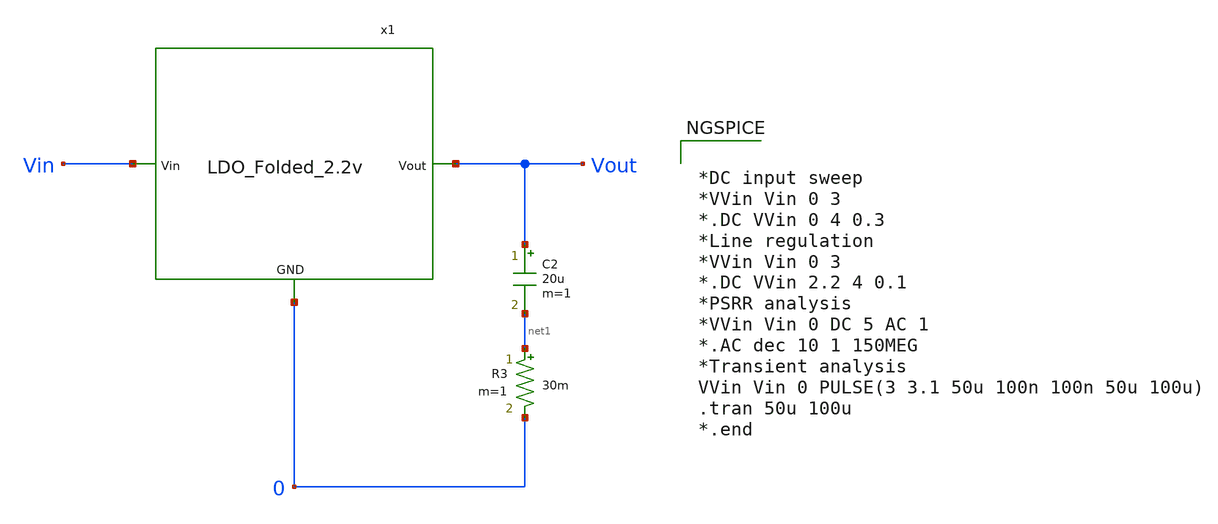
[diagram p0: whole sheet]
** sch_path: Analog_Blocks/LDO/Testbench/LDO_Folded_2.2v_TB.sch
**.subckt LDO_Folded_2.2v_TB
C2 Vout net1 20u m=1
R3 net1 0 30m m=1
x1 Vin Vout 0 LDO_Folded_2.2v
**** begin user architecture code


*DC input sweep
*VVin Vin 0 3
*.DC VVin 0 4 0.3
*Line regulation
*VVin Vin 0 3
*.DC VVin 2.2 4 0.1
*PSRR analysis
*VVin Vin 0 DC 5 AC 1
*.AC dec 10 1 150MEG
*Transient analysis
VVin Vin 0 PULSE(3 3.1 50u 100n 100n 50u 100u)
.tran 50u 100u
*.end



.include $::SKYWATER_MODELS/cells/nfet_01v8/sky130_fd_pr__nfet_01v8__tt.corner.spice
.include $::SKYWATER_MODELS/cells/nfet_01v8_lvt/sky130_fd_pr__nfet_01v8_lvt__tt.corner.spice
.include $::SKYWATER_MODELS/cells/pfet_01v8/sky130_fd_pr__pfet_01v8__tt.corner.spice
.include $::SKYWATER_MODELS/cells/nfet_03v3_nvt/sky130_fd_pr__nfet_03v3_nvt__tt.corner.spice
.include $::SKYWATER_MODELS/cells/nfet_05v0_nvt/sky130_fd_pr__nfet_05v0_nvt__tt.corner.spice
.include $::SKYWATER_MODELS/cells/esd_nfet_01v8/sky130_fd_pr__esd_nfet_01v8__tt.corner.spice
.include $::SKYWATER_MODELS/cells/pfet_01v8_lvt/sky130_fd_pr__pfet_01v8_lvt__tt.corner.spice
.include $::SKYWATER_MODELS/cells/pfet_01v8_hvt/sky130_fd_pr__pfet_01v8_hvt__tt.corner.spice
.include $::SKYWATER_MODELS/cells/esd_pfet_g5v0d10v5/sky130_fd_pr__esd_pfet_g5v0d10v5__tt.corner.spice
.include $::SKYWATER_MODELS/cells/pfet_g5v0d10v5/sky130_fd_pr__pfet_g5v0d10v5__tt.corner.spice
.include $::SKYWATER_MODELS/cells/pfet_g5v0d16v0/sky130_fd_pr__pfet_g5v0d16v0__tt.corner.spice
.include $::SKYWATER_MODELS/cells/nfet_g5v0d10v5/sky130_fd_pr__nfet_g5v0d10v5__tt.corner.spice
.include $::SKYWATER_MODELS/cells/nfet_g5v0d16v0/sky130_fd_pr__nfet_g5v0d16v0__tt_discrete.corner.spice
.include $::SKYWATER_MODELS/cells/esd_nfet_g5v0d10v5/sky130_fd_pr__esd_nfet_g5v0d10v5__tt.corner.spice
.include $::SKYWATER_MODELS/models/corners/tt/nonfet.spice
* Mismatch parameters
.include $::SKYWATER_MODELS/cells/nfet_01v8/sky130_fd_pr__nfet_01v8__mismatch.corner.spice
.include $::SKYWATER_MODELS/cells/pfet_01v8/sky130_fd_pr__pfet_01v8__mismatch.corner.spice
.include $::SKYWATER_MODELS/cells/nfet_01v8_lvt/sky130_fd_pr__nfet_01v8_lvt__mismatch.corner.spice
.include $::SKYWATER_MODELS/cells/pfet_01v8_lvt/sky130_fd_pr__pfet_01v8_lvt__mismatch.corner.spice
.include $::SKYWATER_MODELS/cells/pfet_01v8_hvt/sky130_fd_pr__pfet_01v8_hvt__mismatch.corner.spice
.include $::SKYWATER_MODELS/cells/nfet_g5v0d10v5/sky130_fd_pr__nfet_g5v0d10v5__mismatch.corner.spice
.include $::SKYWATER_MODELS/cells/pfet_g5v0d10v5/sky130_fd_pr__pfet_g5v0d10v5__mismatch.corner.spice
.include $::SKYWATER_MODELS/cells/nfet_05v0_nvt/sky130_fd_pr__nfet_05v0_nvt__mismatch.corner.spice
.include $::SKYWATER_MODELS/cells/nfet_03v3_nvt/sky130_fd_pr__nfet_03v3_nvt__mismatch.corner.spice
* Resistor$::SKYWATER_MODELS/Capacitor
.include $::SKYWATER_MODELS/models/r+c/res_typical__cap_typical.spice
.include $::SKYWATER_MODELS/models/r+c/res_typical__cap_typical__lin.spice
* Special cells
.include $::SKYWATER_MODELS/models/corners/tt/specialized_cells.spice
* All models
.include $::SKYWATER_MODELS/models/all.spice
* Corner
.include $::SKYWATER_MODELS/models/corners/tt/rf.spice

**** end user architecture code
**.ends

* expanding   symbol:
*+  /home/eslam/Analog_blocks/Analog_Blocks/LDO/Schematic/LDO_Folded_2.2v/LDO_Folded_2.2v.sym # of pins=3
** sym_path: Analog_blocks/Analog_Blocks/LDO/Schematic/LDO_Folded_2.2v/LDO_Folded_2.2v.sym
** sch_path: Analog_blocks/Analog_Blocks/LDO/Schematic/LDO_Folded_2.2v/LDO_Folded_2.2v.sch
.subckt LDO_Folded_2.2v Vin Vout GND
*.ipin Vin
*.ipin GND
*.opin Vout
XR1 net1 Vout GND sky130_fd_pr__res_xhigh_po W=1 L=60 mult=1 m=1
XR2 GND net1 GND sky130_fd_pr__res_xhigh_po W=1 L=50 mult=1 m=1
XC1 Vout net1 sky130_fd_pr__cap_mim_m3_2 W=1 L=1 MF=1 m=1
XM1 Vout net2 Vin Vin sky130_fd_pr__pfet_g5v0d10v5 L=0.5 W=20 nf=1 ad='int((nf+1)/2) * W/nf * 0.29' as='int((nf+2)/2) * W/nf * 0.29'
+ pd='2*int((nf+1)/2) * (W/nf + 0.29)' ps='2*int((nf+2)/2) * (W/nf + 0.29)' nrd='0.29 / W' nrs='0.29 / W'
+ sa=0 sb=0 sd=0 mult=1000 m=1000
x1 Vin net2 net1 net3 net3 GND Error_amplifier_Folded
x2 net3 Vin GND Bandgap5v
.ends


* expanding   symbol:
*+  /home/eslam/Analog_blocks/Analog_Blocks/LDO/Schematic/LDO_Folded_2.2v/Error_amplifier_Folded.sym # of pins=6
** sym_path: Analog_Blocks/LDO/Schematic/LDO_Folded_1.8v/Error_amplifier_Folded.sym
** sch_path: Analog_Blocks/LDO/Schematic/LDO_Folded_1.8v/Error_amplifier_Folded.sch
.subckt Error_amplifier_Folded VDD Vout Vp Vn Ibias GND
*.ipin VDD
*.ipin GND
*.ipin Vp
*.ipin Vn
*.opin Vout
*.ipin Ibias
XM1 net3 Vp net1 GND sky130_fd_pr__nfet_g5v0d10v5 L=0.5 W=50 nf=1 ad='int((nf+1)/2) * W/nf * 0.29' as='int((nf+2)/2) * W/nf * 0.29'
+ pd='2*int((nf+1)/2) * (W/nf + 0.29)' ps='2*int((nf+2)/2) * (W/nf + 0.29)' nrd='0.29 / W' nrs='0.29 / W'
+ sa=0 sb=0 sd=0 mult=1 m=1
XM2 net2 Vn net1 GND sky130_fd_pr__nfet_g5v0d10v5 L=0.5 W=50 nf=1 ad='int((nf+1)/2) * W/nf * 0.29' as='int((nf+2)/2) * W/nf * 0.29'
+ pd='2*int((nf+1)/2) * (W/nf + 0.29)' ps='2*int((nf+2)/2) * (W/nf + 0.29)' nrd='0.29 / W' nrs='0.29 / W'
+ sa=0 sb=0 sd=0 mult=1 m=1
XM9 Vout net4 GND GND sky130_fd_pr__nfet_g5v0d10v5 L=2 W=6 nf=1 ad='int((nf+1)/2) * W/nf * 0.29' as='int((nf+2)/2) * W/nf * 0.29'
+ pd='2*int((nf+1)/2) * (W/nf + 0.29)' ps='2*int((nf+2)/2) * (W/nf + 0.29)' nrd='0.29 / W' nrs='0.29 / W'
+ sa=0 sb=0 sd=0 mult=1 m=1
XM6 net4 net6 net3 VDD sky130_fd_pr__pfet_g5v0d10v5 L=0.5 W=40 nf=1 ad='int((nf+1)/2) * W/nf * 0.29'
+ as='int((nf+2)/2) * W/nf * 0.29' pd='2*int((nf+1)/2) * (W/nf + 0.29)' ps='2*int((nf+2)/2) * (W/nf + 0.29)'
+ nrd='0.29 / W' nrs='0.29 / W' sa=0 sb=0 sd=0 mult=1 m=1
XM5 net2 net5 VDD VDD sky130_fd_pr__pfet_g5v0d10v5 L=0.5 W=40 nf=1 ad='int((nf+1)/2) * W/nf * 0.29' as='int((nf+2)/2) * W/nf * 0.29'
+ pd='2*int((nf+1)/2) * (W/nf + 0.29)' ps='2*int((nf+2)/2) * (W/nf + 0.29)' nrd='0.29 / W' nrs='0.29 / W'
+ sa=0 sb=0 sd=0 mult=1 m=1
XM4 net3 net5 VDD VDD sky130_fd_pr__pfet_g5v0d10v5 L=0.5 W=40 nf=1 ad='int((nf+1)/2) * W/nf * 0.29' as='int((nf+2)/2) * W/nf * 0.29'
+ pd='2*int((nf+1)/2) * (W/nf + 0.29)' ps='2*int((nf+2)/2) * (W/nf + 0.29)' nrd='0.29 / W' nrs='0.29 / W'
+ sa=0 sb=0 sd=0 mult=1 m=1
XM3 net1 Ibias GND GND sky130_fd_pr__nfet_g5v0d10v5 L=0.9 W=12 nf=1 ad='int((nf+1)/2) * W/nf * 0.29'
+ as='int((nf+2)/2) * W/nf * 0.29' pd='2*int((nf+1)/2) * (W/nf + 0.29)' ps='2*int((nf+2)/2) * (W/nf + 0.29)'
+ nrd='0.29 / W' nrs='0.29 / W' sa=0 sb=0 sd=0 mult=1 m=1
XM7 Vout net6 net2 VDD sky130_fd_pr__pfet_g5v0d10v5 L=0.5 W=40 nf=1 ad='int((nf+1)/2) * W/nf * 0.29'
+ as='int((nf+2)/2) * W/nf * 0.29' pd='2*int((nf+1)/2) * (W/nf + 0.29)' ps='2*int((nf+2)/2) * (W/nf + 0.29)'
+ nrd='0.29 / W' nrs='0.29 / W' sa=0 sb=0 sd=0 mult=1 m=1
XM8 net4 net4 GND GND sky130_fd_pr__nfet_g5v0d10v5 L=2 W=6 nf=1 ad='int((nf+1)/2) * W/nf * 0.29' as='int((nf+2)/2) * W/nf * 0.29'
+ pd='2*int((nf+1)/2) * (W/nf + 0.29)' ps='2*int((nf+2)/2) * (W/nf + 0.29)' nrd='0.29 / W' nrs='0.29 / W'
+ sa=0 sb=0 sd=0 mult=1 m=1
XM10 Ibias Ibias GND GND sky130_fd_pr__nfet_g5v0d10v5 L=0.9 W=12 nf=1 ad='int((nf+1)/2) * W/nf * 0.29'
+ as='int((nf+2)/2) * W/nf * 0.29' pd='2*int((nf+1)/2) * (W/nf + 0.29)' ps='2*int((nf+2)/2) * (W/nf + 0.29)'
+ nrd='0.29 / W' nrs='0.29 / W' sa=0 sb=0 sd=0 mult=1 m=1
XM11 net5 Ibias GND GND sky130_fd_pr__nfet_g5v0d10v5 L=0.9 W=6 nf=1 ad='int((nf+1)/2) * W/nf * 0.29'
+ as='int((nf+2)/2) * W/nf * 0.29' pd='2*int((nf+1)/2) * (W/nf + 0.29)' ps='2*int((nf+2)/2) * (W/nf + 0.29)'
+ nrd='0.29 / W' nrs='0.29 / W' sa=0 sb=0 sd=0 mult=1 m=1
XM12 net6 Ibias GND GND sky130_fd_pr__nfet_g5v0d10v5 L=0.9 W=6 nf=1 ad='int((nf+1)/2) * W/nf * 0.29'
+ as='int((nf+2)/2) * W/nf * 0.29' pd='2*int((nf+1)/2) * (W/nf + 0.29)' ps='2*int((nf+2)/2) * (W/nf + 0.29)'
+ nrd='0.29 / W' nrs='0.29 / W' sa=0 sb=0 sd=0 mult=1 m=1
XM13 net5 net5 VDD VDD sky130_fd_pr__pfet_g5v0d10v5 L=0.5 W=13.5 nf=1 ad='int((nf+1)/2) * W/nf * 0.29'
+ as='int((nf+2)/2) * W/nf * 0.29' pd='2*int((nf+1)/2) * (W/nf + 0.29)' ps='2*int((nf+2)/2) * (W/nf + 0.29)'
+ nrd='0.29 / W' nrs='0.29 / W' sa=0 sb=0 sd=0 mult=1 m=1
XM14 net6 net6 VDD VDD sky130_fd_pr__pfet_g5v0d10v5 L=1 W=2 nf=1 ad='int((nf+1)/2) * W/nf * 0.29' as='int((nf+2)/2) * W/nf * 0.29'
+ pd='2*int((nf+1)/2) * (W/nf + 0.29)' ps='2*int((nf+2)/2) * (W/nf + 0.29)' nrd='0.29 / W' nrs='0.29 / W'
+ sa=0 sb=0 sd=0 mult=1 m=1
.ends


* expanding   symbol:
*+  /home/eslam/Analog_blocks/Analog_Blocks/LDO/Schematic/LDO_Folded_2.2v/Bandgap5v.sym # of pins=3
** sym_path: Analog_Blocks/Bandgap/Schematics/BGR5v/Bandgap5v.sym
** sch_path: Analog_Blocks/Bandgap/Schematics/BGR5v/Bandgap5v.sch
.subckt Bandgap5v Vref VDD GND
*.ipin VDD
*.ipin GND
*.opin Vref
XQ1 GND GND net3 sky130_fd_pr__pnp_05v5_W0p68L0p68 m=1
XQ2 GND GND net1 sky130_fd_pr__pnp_05v5_W0p68L0p68 m=1
XQ3 GND GND net1 sky130_fd_pr__pnp_05v5_W0p68L0p68 m=1
XQ4 GND GND net1 sky130_fd_pr__pnp_05v5_W0p68L0p68 m=1
XQ5 GND GND net1 sky130_fd_pr__pnp_05v5_W0p68L0p68 m=1
XQ6 GND GND net1 sky130_fd_pr__pnp_05v5_W0p68L0p68 m=1
XQ7 GND GND net1 sky130_fd_pr__pnp_05v5_W0p68L0p68 m=1
XQ8 GND GND net1 sky130_fd_pr__pnp_05v5_W0p68L0p68 m=1
XQ9 GND GND net1 sky130_fd_pr__pnp_05v5_W0p68L0p68 m=1
XM2 net4 net5 VDD VDD sky130_fd_pr__pfet_g5v0d10v5 L=1 W=10 nf=1 ad='int((nf+1)/2) * W/nf * 0.29' as='int((nf+2)/2) * W/nf * 0.29'
+ pd='2*int((nf+1)/2) * (W/nf + 0.29)' ps='2*int((nf+2)/2) * (W/nf + 0.29)' nrd='0.29 / W' nrs='0.29 / W'
+ sa=0 sb=0 sd=0 mult=1 m=1
XM3 net3 net4 VDD VDD sky130_fd_pr__pfet_g5v0d10v5 L=1 W=10 nf=1 ad='int((nf+1)/2) * W/nf * 0.29' as='int((nf+2)/2) * W/nf * 0.29'
+ pd='2*int((nf+1)/2) * (W/nf + 0.29)' ps='2*int((nf+2)/2) * (W/nf + 0.29)' nrd='0.29 / W' nrs='0.29 / W'
+ sa=0 sb=0 sd=0 mult=1 m=1
XM1 net4 net5 GND GND sky130_fd_pr__nfet_g5v0d10v5 L=40 W=1 nf=1 ad='int((nf+1)/2) * W/nf * 0.29' as='int((nf+2)/2) * W/nf * 0.29'
+ pd='2*int((nf+1)/2) * (W/nf + 0.29)' ps='2*int((nf+2)/2) * (W/nf + 0.29)' nrd='0.29 / W' nrs='0.29 / W'
+ sa=0 sb=0 sd=0 mult=1 m=1
XR1 net2 Vref GND sky130_fd_pr__res_high_po W=1 L=6 mult=1 m=1
XR3 net3 Vref GND sky130_fd_pr__res_high_po W=1 L=6 mult=1 m=1
XR2 net1 net2 GND sky130_fd_pr__res_high_po W=1 L=2.6 mult=1 m=1
x1 VDD net3 net2 Vref net5 GND Bandgap5v_OTA
.ends


* expanding   symbol:
*+  /home/eslam/Analog_blocks/Analog_Blocks/Bandgap/Schematics/BGR5v/Bandgap5v_OTA.sym # of pins=6
** sym_path: LDO/Schematic/Bandgap5v_OTA.sym
** sch_path: LDO/Schematic/Bandgap5v_OTA.sch
.subckt Bandgap5v_OTA Vdd Vn Vp Ibias Vhigh Gnd
*.opin Ibias
*.ipin Vhigh
*.ipin Vdd
*.ipin Gnd
*.ipin Vn
*.ipin Vp
XM6 Ibias Vhigh Vdd Vdd sky130_fd_pr__pfet_g5v0d10v5 L=1 W=10 nf=1 ad='int((nf+1)/2) * W/nf * 0.29' as='int((nf+2)/2) * W/nf * 0.29'
+ pd='2*int((nf+1)/2) * (W/nf + 0.29)' ps='2*int((nf+2)/2) * (W/nf + 0.29)' nrd='0.29 / W' nrs='0.29 / W'
+ sa=0 sb=0 sd=0 mult=1 m=1
XM5 net3 Vhigh Vdd Vdd sky130_fd_pr__pfet_g5v0d10v5 L=1 W=10 nf=1 ad='int((nf+1)/2) * W/nf * 0.29' as='int((nf+2)/2) * W/nf * 0.29'
+ pd='2*int((nf+1)/2) * (W/nf + 0.29)' ps='2*int((nf+2)/2) * (W/nf + 0.29)' nrd='0.29 / W' nrs='0.29 / W'
+ sa=0 sb=0 sd=0 mult=1 m=1
XM7 Vhigh Vhigh Vdd Vdd sky130_fd_pr__pfet_g5v0d10v5 L=1 W=54 nf=1 ad='int((nf+1)/2) * W/nf * 0.29' as='int((nf+2)/2) * W/nf * 0.29'
+ pd='2*int((nf+1)/2) * (W/nf + 0.29)' ps='2*int((nf+2)/2) * (W/nf + 0.29)' nrd='0.29 / W' nrs='0.29 / W'
+ sa=0 sb=0 sd=0 mult=1 m=1
XM2 net1 Vp net3 Vdd sky130_fd_pr__pfet_g5v0d10v5 L=1 W=30 nf=1 ad='int((nf+1)/2) * W/nf * 0.29' as='int((nf+2)/2) * W/nf * 0.29'
+ pd='2*int((nf+1)/2) * (W/nf + 0.29)' ps='2*int((nf+2)/2) * (W/nf + 0.29)' nrd='0.29 / W' nrs='0.29 / W'
+ sa=0 sb=0 sd=0 mult=1 m=1
XM1 net2 Vn net3 Vdd sky130_fd_pr__pfet_g5v0d10v5 L=1 W=30 nf=1 ad='int((nf+1)/2) * W/nf * 0.29' as='int((nf+2)/2) * W/nf * 0.29'
+ pd='2*int((nf+1)/2) * (W/nf + 0.29)' ps='2*int((nf+2)/2) * (W/nf + 0.29)' nrd='0.29 / W' nrs='0.29 / W'
+ sa=0 sb=0 sd=0 mult=1 m=1
XM8 Vhigh net1 Gnd Gnd sky130_fd_pr__nfet_g5v0d10v5 L=0.5 W=75 nf=1 ad='int((nf+1)/2) * W/nf * 0.29'
+ as='int((nf+2)/2) * W/nf * 0.29' pd='2*int((nf+1)/2) * (W/nf + 0.29)' ps='2*int((nf+2)/2) * (W/nf + 0.29)'
+ nrd='0.29 / W' nrs='0.29 / W' sa=0 sb=0 sd=0 mult=1 m=1
XM4 net1 net2 Gnd Gnd sky130_fd_pr__nfet_g5v0d10v5 L=0.5 W=7.5 nf=1 ad='int((nf+1)/2) * W/nf * 0.29'
+ as='int((nf+2)/2) * W/nf * 0.29' pd='2*int((nf+1)/2) * (W/nf + 0.29)' ps='2*int((nf+2)/2) * (W/nf + 0.29)'
+ nrd='0.29 / W' nrs='0.29 / W' sa=0 sb=0 sd=0 mult=1 m=1
XM3 net2 net2 Gnd Gnd sky130_fd_pr__nfet_g5v0d10v5 L=0.5 W=7.5 nf=1 ad='int((nf+1)/2) * W/nf * 0.29'
+ as='int((nf+2)/2) * W/nf * 0.29' pd='2*int((nf+1)/2) * (W/nf + 0.29)' ps='2*int((nf+2)/2) * (W/nf + 0.29)'
+ nrd='0.29 / W' nrs='0.29 / W' sa=0 sb=0 sd=0 mult=1 m=1
XC1 net1 Vhigh sky130_fd_pr__cap_mim_m3_2 W=1 L=1 MF=1 m=1
.ends

.end
